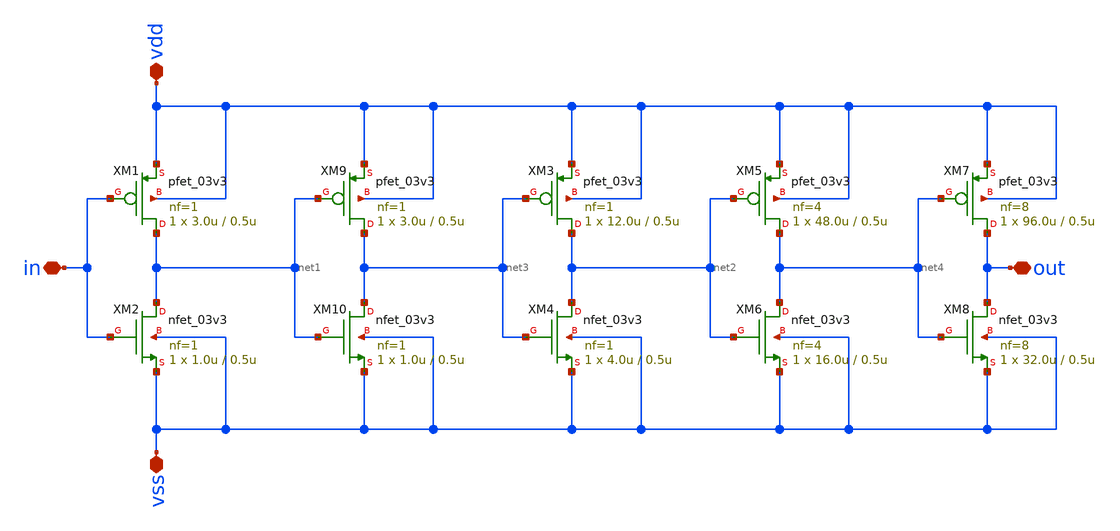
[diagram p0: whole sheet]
** sch_path: designs/libs/core_analog/asc_drive_buffer_up/asc_drive_buffer_up.sch
**.subckt asc_drive_buffer_up in out vss vdd
*.iopin in
*.iopin out
*.iopin vss
*.iopin vdd
XM1 net1 in vdd vdd pfet_03v3 L=0.5u W=3.0u nf=1 ad='int((nf+1)/2) * W/nf * 0.18u' as='int((nf+2)/2) * W/nf * 0.18u'
+ pd='2*int((nf+1)/2) * (W/nf + 0.18u)' ps='2*int((nf+2)/2) * (W/nf + 0.18u)' nrd='0.18u / W' nrs='0.18u / W'
+ sa=0 sb=0 sd=0 m=1
XM2 net1 in vss vss nfet_03v3 L=0.5u W=1.0u nf=1 ad='int((nf+1)/2) * W/nf * 0.18u' as='int((nf+2)/2) * W/nf * 0.18u'
+ pd='2*int((nf+1)/2) * (W/nf + 0.18u)' ps='2*int((nf+2)/2) * (W/nf + 0.18u)' nrd='0.18u / W' nrs='0.18u / W'
+ sa=0 sb=0 sd=0 m=1
XM3 net2 net3 vdd vdd pfet_03v3 L=0.5u W=12.0u nf=1 ad='int((nf+1)/2) * W/nf * 0.18u' as='int((nf+2)/2) * W/nf * 0.18u'
+ pd='2*int((nf+1)/2) * (W/nf + 0.18u)' ps='2*int((nf+2)/2) * (W/nf + 0.18u)' nrd='0.18u / W' nrs='0.18u / W'
+ sa=0 sb=0 sd=0 m=1
XM4 net2 net3 vss vss nfet_03v3 L=0.5u W=4.0u nf=1 ad='int((nf+1)/2) * W/nf * 0.18u' as='int((nf+2)/2) * W/nf * 0.18u'
+ pd='2*int((nf+1)/2) * (W/nf + 0.18u)' ps='2*int((nf+2)/2) * (W/nf + 0.18u)' nrd='0.18u / W' nrs='0.18u / W'
+ sa=0 sb=0 sd=0 m=1
XM5 net4 net2 vdd vdd pfet_03v3 L=0.5u W=48.0u nf=4 ad='int((nf+1)/2) * W/nf * 0.18u' as='int((nf+2)/2) * W/nf * 0.18u'
+ pd='2*int((nf+1)/2) * (W/nf + 0.18u)' ps='2*int((nf+2)/2) * (W/nf + 0.18u)' nrd='0.18u / W' nrs='0.18u / W'
+ sa=0 sb=0 sd=0 m=1
XM6 net4 net2 vss vss nfet_03v3 L=0.5u W=16.0u nf=4 ad='int((nf+1)/2) * W/nf * 0.18u' as='int((nf+2)/2) * W/nf * 0.18u'
+ pd='2*int((nf+1)/2) * (W/nf + 0.18u)' ps='2*int((nf+2)/2) * (W/nf + 0.18u)' nrd='0.18u / W' nrs='0.18u / W'
+ sa=0 sb=0 sd=0 m=1
XM7 out net4 vdd vdd pfet_03v3 L=0.5u W=96.0u nf=8 ad='int((nf+1)/2) * W/nf * 0.18u' as='int((nf+2)/2) * W/nf * 0.18u'
+ pd='2*int((nf+1)/2) * (W/nf + 0.18u)' ps='2*int((nf+2)/2) * (W/nf + 0.18u)' nrd='0.18u / W' nrs='0.18u / W'
+ sa=0 sb=0 sd=0 m=1
XM8 out net4 vss vss nfet_03v3 L=0.5u W=32.0u nf=8 ad='int((nf+1)/2) * W/nf * 0.18u' as='int((nf+2)/2) * W/nf * 0.18u'
+ pd='2*int((nf+1)/2) * (W/nf + 0.18u)' ps='2*int((nf+2)/2) * (W/nf + 0.18u)' nrd='0.18u / W' nrs='0.18u / W'
+ sa=0 sb=0 sd=0 m=1
XM9 net3 net1 vdd vdd pfet_03v3 L=0.5u W=3.0u nf=1 ad='int((nf+1)/2) * W/nf * 0.18u' as='int((nf+2)/2) * W/nf * 0.18u'
+ pd='2*int((nf+1)/2) * (W/nf + 0.18u)' ps='2*int((nf+2)/2) * (W/nf + 0.18u)' nrd='0.18u / W' nrs='0.18u / W'
+ sa=0 sb=0 sd=0 m=1
XM10 net3 net1 vss vss nfet_03v3 L=0.5u W=1.0u nf=1 ad='int((nf+1)/2) * W/nf * 0.18u' as='int((nf+2)/2) * W/nf * 0.18u'
+ pd='2*int((nf+1)/2) * (W/nf + 0.18u)' ps='2*int((nf+2)/2) * (W/nf + 0.18u)' nrd='0.18u / W' nrs='0.18u / W'
+ sa=0 sb=0 sd=0 m=1
**.ends
.end
